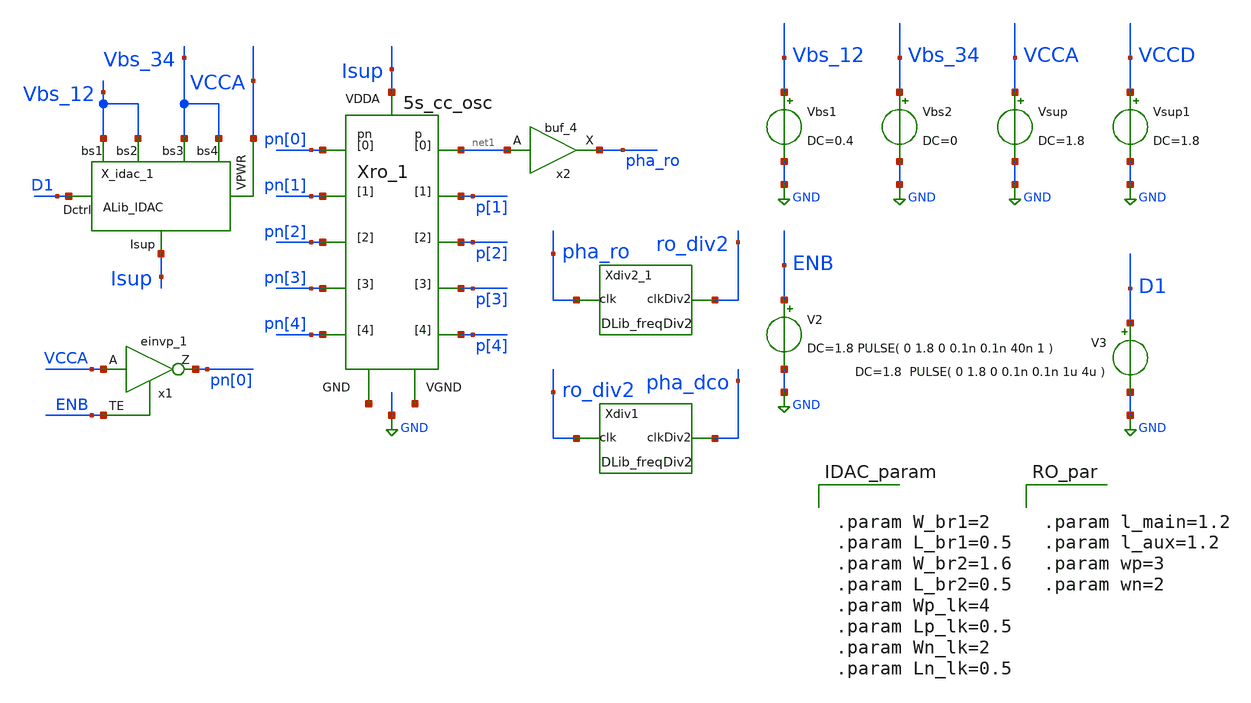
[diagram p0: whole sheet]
** sch_path: xschem/tb/IDAC_tb.sch

.include $::SKYWATER_STDCELLS/sky130_fd_sc_hd.spice
.lib $::SKYWATER_MODELS/sky130.lib.spice tt

**.subckt IDAC_tb
Vsup VCCA GND DC=1.8
Vbs1 Vbs_12 GND DC=0.4
x1 VCCA ENB VGND VNB VPB VPWR pn[0] sky130_fd_sc_hd__einvp_1
V2 ENB GND DC=1.8 PULSE( 0 1.8 0 0.1n 0.1n 40n 1 )
V3 D1 GND DC=1.8 PULSE( 0 1.8 0 0.1n 0.1n 1u 4u )
X_idac_1 D1 Vbs_12 Vbs_12 Vbs_34 Vbs_34 VCCA Isup ALib_IDAC W_br1="W_br1" L_br1="L_br1"
+ W_br2="W_br2" L_br2="L_br2" Wp_lk="Wp_lk" Lp_lk="Lp_lk" Wn_lk="Wn_lk" Ln_lk="Wn_lk"
Vbs2 Vbs_34 GND DC=0
x2 net1 GND GND VCCD VCCD pha_ro sky130_fd_sc_hd__buf_4
Vsup1 VCCD GND DC=1.8
Xdiv2_1 pha_ro GND GND VCCD VCCD ro_div2 DLib_freqDiv2
Xro_1 net2 Isup net1 p[1] p[2] p[3] p[4] pn[0] pn[1] pn[2] pn[3] pn[4] net3 5s_cc_osc
Xdiv1 ro_div2 GND GND VCCD VCCD pha_dco DLib_freqDiv2
**** begin user architecture code


.param W_br1=2
.param L_br1=0.5
.param W_br2=1.6
.param L_br2=0.5
.param Wp_lk=4
.param Lp_lk=0.5
.param Wn_lk=2
.param Ln_lk=0.5

**** end user architecture code
**.ends
.GLOBAL GND
**** begin user architecture code


.control
set nobreak
set num_threads=8
set test_mode = 0
* mode = 0: operation testing    1:  frequency extraction    2:  power consumption
if ($test_mode = 0)
    TRAN 1n 12u
    plot pha_ro+4 ro_div2+2 pha_dco
    MEAS TRAN prd TRIG pha_ro VAL=0.8 RISE=10 TARG pha_ro VAL=0.8 RISE=20
    let freq = 10/prd
    echo "frequency: "
    print freq
end

if ($test_mode = 2)
    save vdd @Vsup[i] pha_dco
    TRAN 0.1n 5u
    MEAS TRAN I_vco AVG @Vsup[i] FROM=3u TO=4u
    MEAS TRAN V_vco AVG vdd FROM=3u TO=4u
    let Power=I_vco*V_vco
    print Power
end
.endc




.param l_main=1.2
.param l_aux=1.2
.param wp=3
.param wn=2

**** end user architecture code
.end
